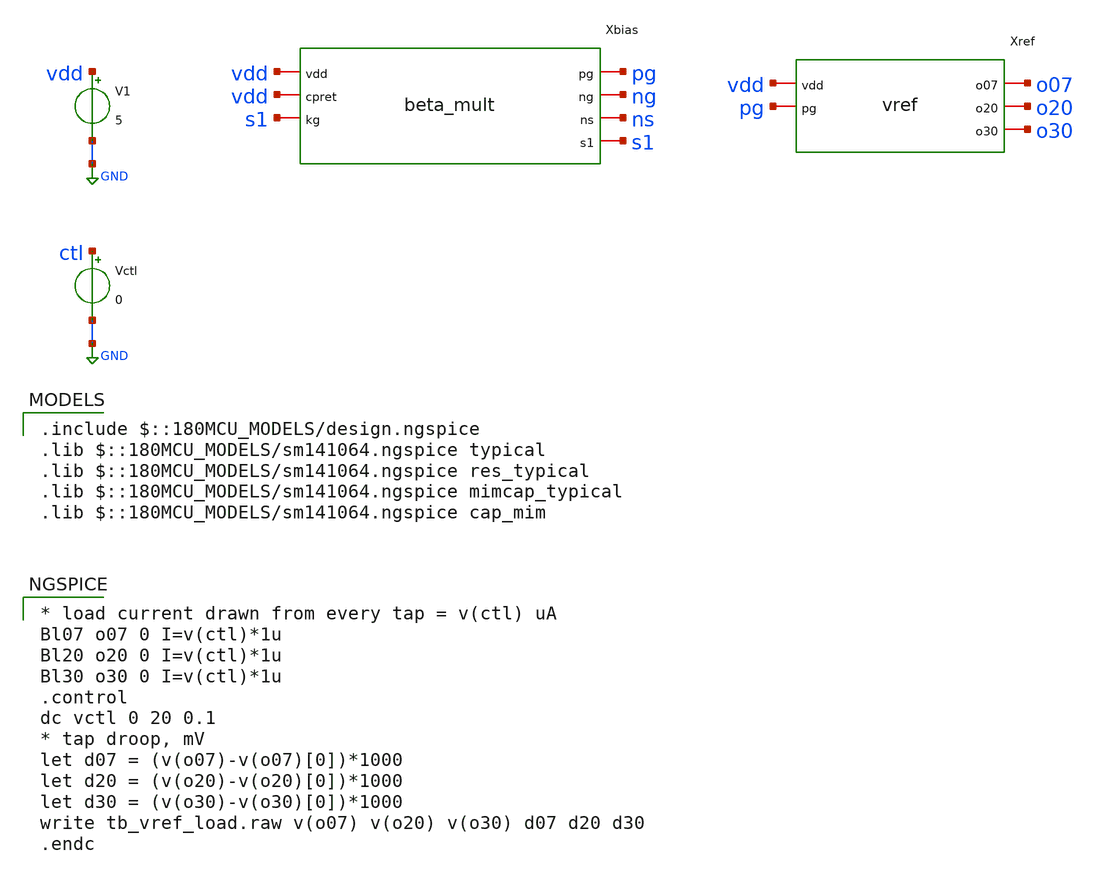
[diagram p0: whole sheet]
** sch_path: Schematics #2/sims/tb/tb_vref_load.sch
**.subckt tb_vref_load
V1 vdd GND 5
Vctl ctl GND 0
Xbias vdd pg ng ns vdd s1 s1 beta_mult
Xref vdd pg o07 o20 o30 vref
**** begin user architecture code
 .include $::180MCU_MODELS/design.ngspice
.lib $::180MCU_MODELS/sm141064.ngspice typical
.lib $::180MCU_MODELS/sm141064.ngspice res_typical
.lib $::180MCU_MODELS/sm141064.ngspice mimcap_typical
.lib $::180MCU_MODELS/sm141064.ngspice cap_mim

* load current drawn from every tap = v(ctl) uA
Bl07 o07 0 I=v(ctl)*1u
Bl20 o20 0 I=v(ctl)*1u
Bl30 o30 0 I=v(ctl)*1u
.control
dc vctl 0 20 0.1
* tap droop, mV
let d07 = (v(o07)-v(o07)[0])*1000
let d20 = (v(o20)-v(o20)[0])*1000
let d30 = (v(o30)-v(o30)[0])*1000
write tb_vref_load.raw v(o07) v(o20) v(o30) d07 d20 d30
.endc

**** end user architecture code
**.ends
.GLOBAL GND
.end
